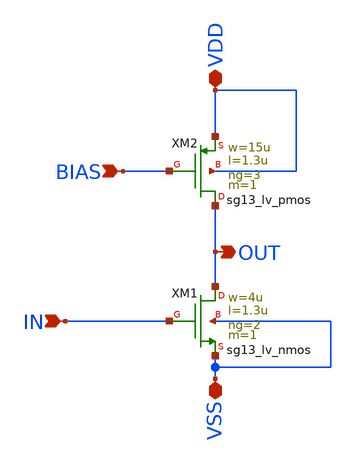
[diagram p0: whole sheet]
** sch_path: BTDay6-Ex/CS_Ampli_Current.sch
**.subckt CS_Ampli_Current OUT IN VDD VSS BIAS
*.opin OUT
*.ipin IN
*.iopin VDD
*.iopin VSS
*.ipin BIAS
XXM1 OUT IN VSS VSS sg13_lv_nmos w=4u l=1.3u ng=2 m=1 mm_ok=1
XXM2 OUT BIAS VDD VDD sg13_lv_pmos w=15u l=1.3u ng=3 m=1 mm_ok=1
**.ends
.end
